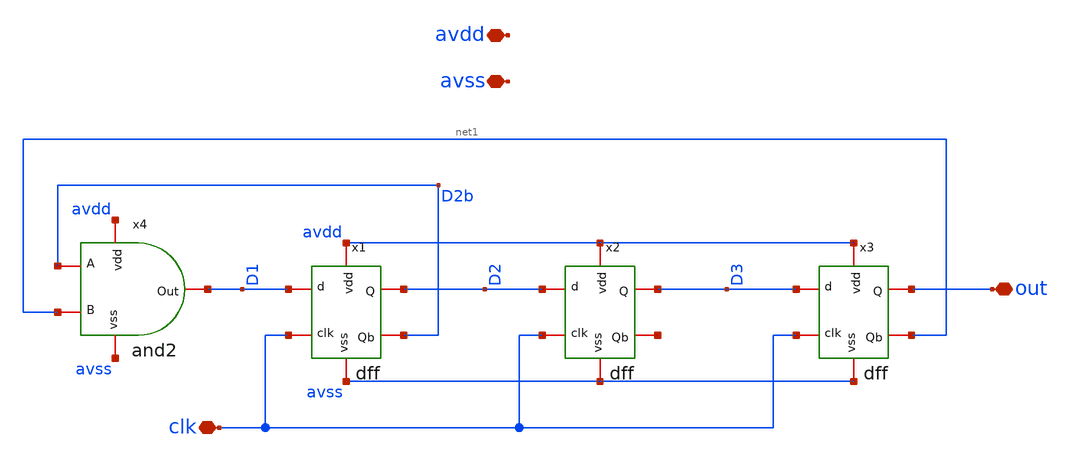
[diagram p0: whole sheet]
** sch_path: designs/libs/adc_singlecycle/adc_singlecycle.sch
**.subckt adc_singlecycle clk out avdd avss
*.iopin clk
*.iopin out
*.iopin avdd
*.iopin avss
x1 D1 D2 avdd avss clk D2b dff
x2 D2 D3 avdd avss clk net2 dff
x3 D3 out avdd avss clk net1 dff
x4 avdd net1 D2b D1 avss and2
**.ends
.end
